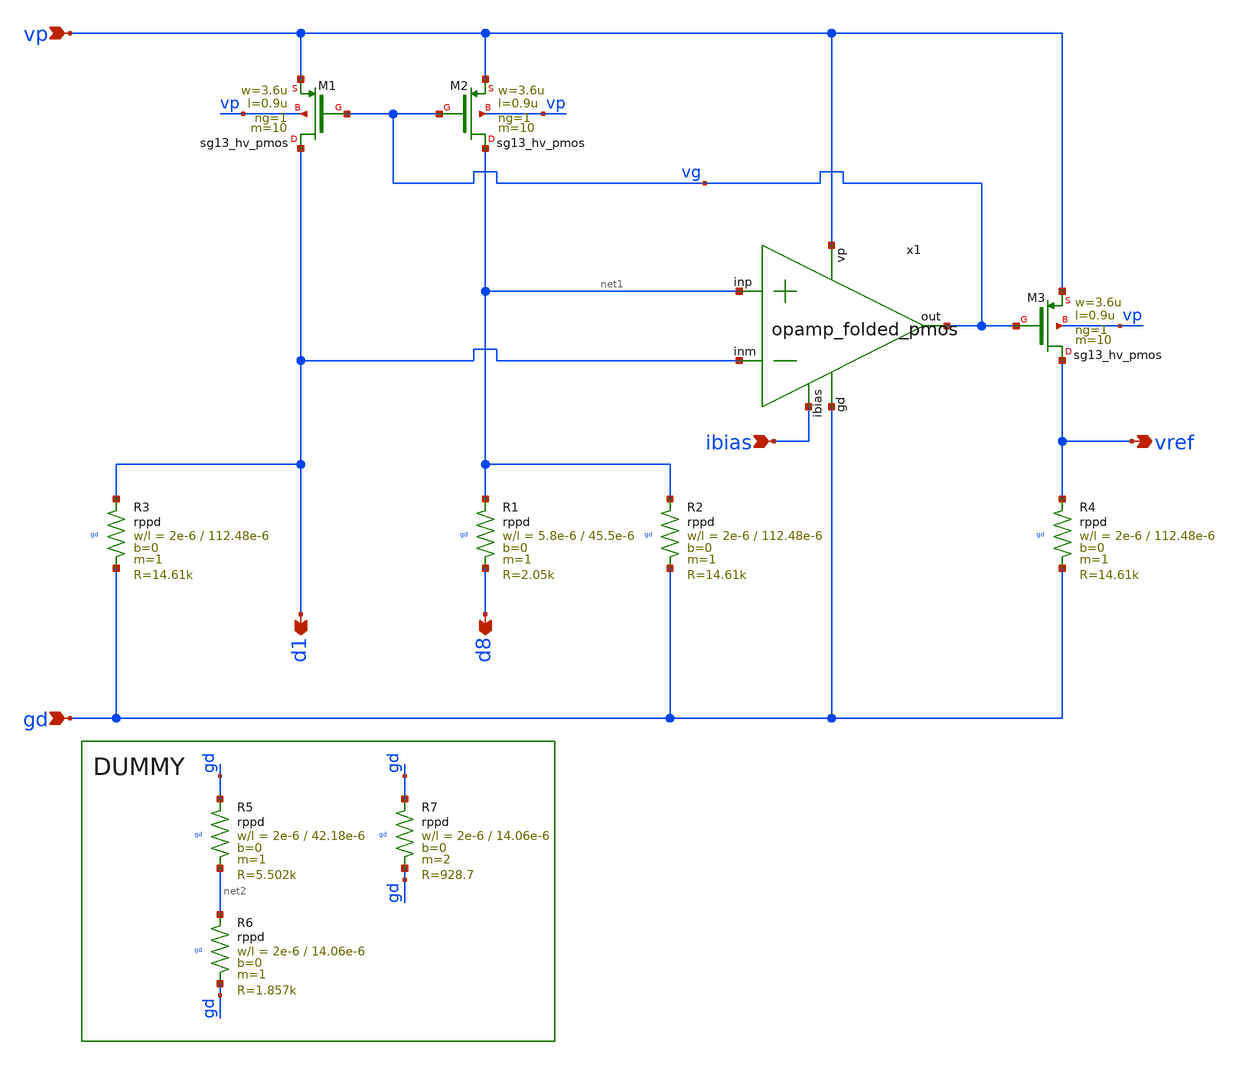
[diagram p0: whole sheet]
** sch_path: PLL0663-main/schematic/xschem/bandgap/bandgap_res_core.sch
**.subckt bandgap_res_core gd vp ibias vref d1 d8
*.ipin gd
*.ipin vp
*.ipin ibias
*.opin vref
*.opin d1
*.opin d8
XM2 net1 vg vp vp sg13_hv_pmos w=3.6u l=0.9u ng=1 m=10 mm_ok=1
XM1 d1 vg vp vp sg13_hv_pmos w=3.6u l=0.9u ng=1 m=10 mm_ok=1
XM3 vref vg vp vp sg13_hv_pmos w=3.6u l=0.9u ng=1 m=10 mm_ok=1
XR2 net1 gd gd rppd w=2e-6 l=112.48e-6 m=1 b=0 mm_ok=1
XR3 d1 gd gd rppd w=2e-6 l=112.48e-6 m=1 b=0 mm_ok=1
XR4 vref gd gd rppd w=2e-6 l=112.48e-6 m=1 b=0 mm_ok=1
XR1 net1 d8 gd rppd w=5.8e-6 l=45.5e-6 m=1 b=0 mm_ok=1
XR5 gd net2 gd rppd w=2e-6 l=42.18e-6 m=1 b=0 mm_ok=1
XR6 net2 gd gd rppd w=2e-6 l=14.06e-6 m=1 b=0 mm_ok=1
XR7 gd gd gd rppd w=2e-6 l=14.06e-6 m=2 b=0 mm_ok=1
x1 vp net1 d1 vg ibias gd opamp_folded_pmos
**.ends
.end
